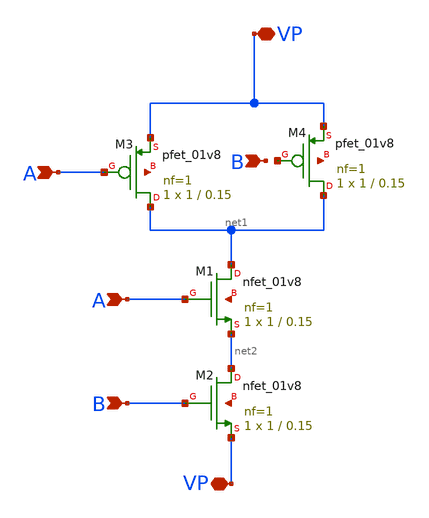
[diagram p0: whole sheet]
** sch_path: AND_Gate.sch
**.subckt AND_Gate VP VP A A B B
*.iopin VP
*.iopin VP
*.ipin A
*.ipin A
*.ipin B
*.ipin B
XM1 net1 A net2 net3 sky130_fd_pr__nfet_01v8 L=0.15 W=1 nf=1 ad='int((nf+1)/2) * W/nf * 0.29' as='int((nf+2)/2) * W/nf * 0.29'
+ pd='2*int((nf+1)/2) * (W/nf + 0.29)' ps='2*int((nf+2)/2) * (W/nf + 0.29)' nrd='0.29 / W' nrs='0.29 / W'
+ sa=0 sb=0 sd=0 mult=1 m=1
XM2 net2 B VP net4 sky130_fd_pr__nfet_01v8 L=0.15 W=1 nf=1 ad='int((nf+1)/2) * W/nf * 0.29' as='int((nf+2)/2) * W/nf * 0.29'
+ pd='2*int((nf+1)/2) * (W/nf + 0.29)' ps='2*int((nf+2)/2) * (W/nf + 0.29)' nrd='0.29 / W' nrs='0.29 / W'
+ sa=0 sb=0 sd=0 mult=1 m=1
XM3 net1 A VP net5 sky130_fd_pr__pfet_01v8 L=0.15 W=1 nf=1 ad='int((nf+1)/2) * W/nf * 0.29' as='int((nf+2)/2) * W/nf * 0.29'
+ pd='2*int((nf+1)/2) * (W/nf + 0.29)' ps='2*int((nf+2)/2) * (W/nf + 0.29)' nrd='0.29 / W' nrs='0.29 / W'
+ sa=0 sb=0 sd=0 mult=1 m=1
XM4 net1 net6 VP net7 sky130_fd_pr__pfet_01v8 L=0.15 W=1 nf=1 ad='int((nf+1)/2) * W/nf * 0.29' as='int((nf+2)/2) * W/nf * 0.29'
+ pd='2*int((nf+1)/2) * (W/nf + 0.29)' ps='2*int((nf+2)/2) * (W/nf + 0.29)' nrd='0.29 / W' nrs='0.29 / W'
+ sa=0 sb=0 sd=0 mult=1 m=1
**.ends
.end
